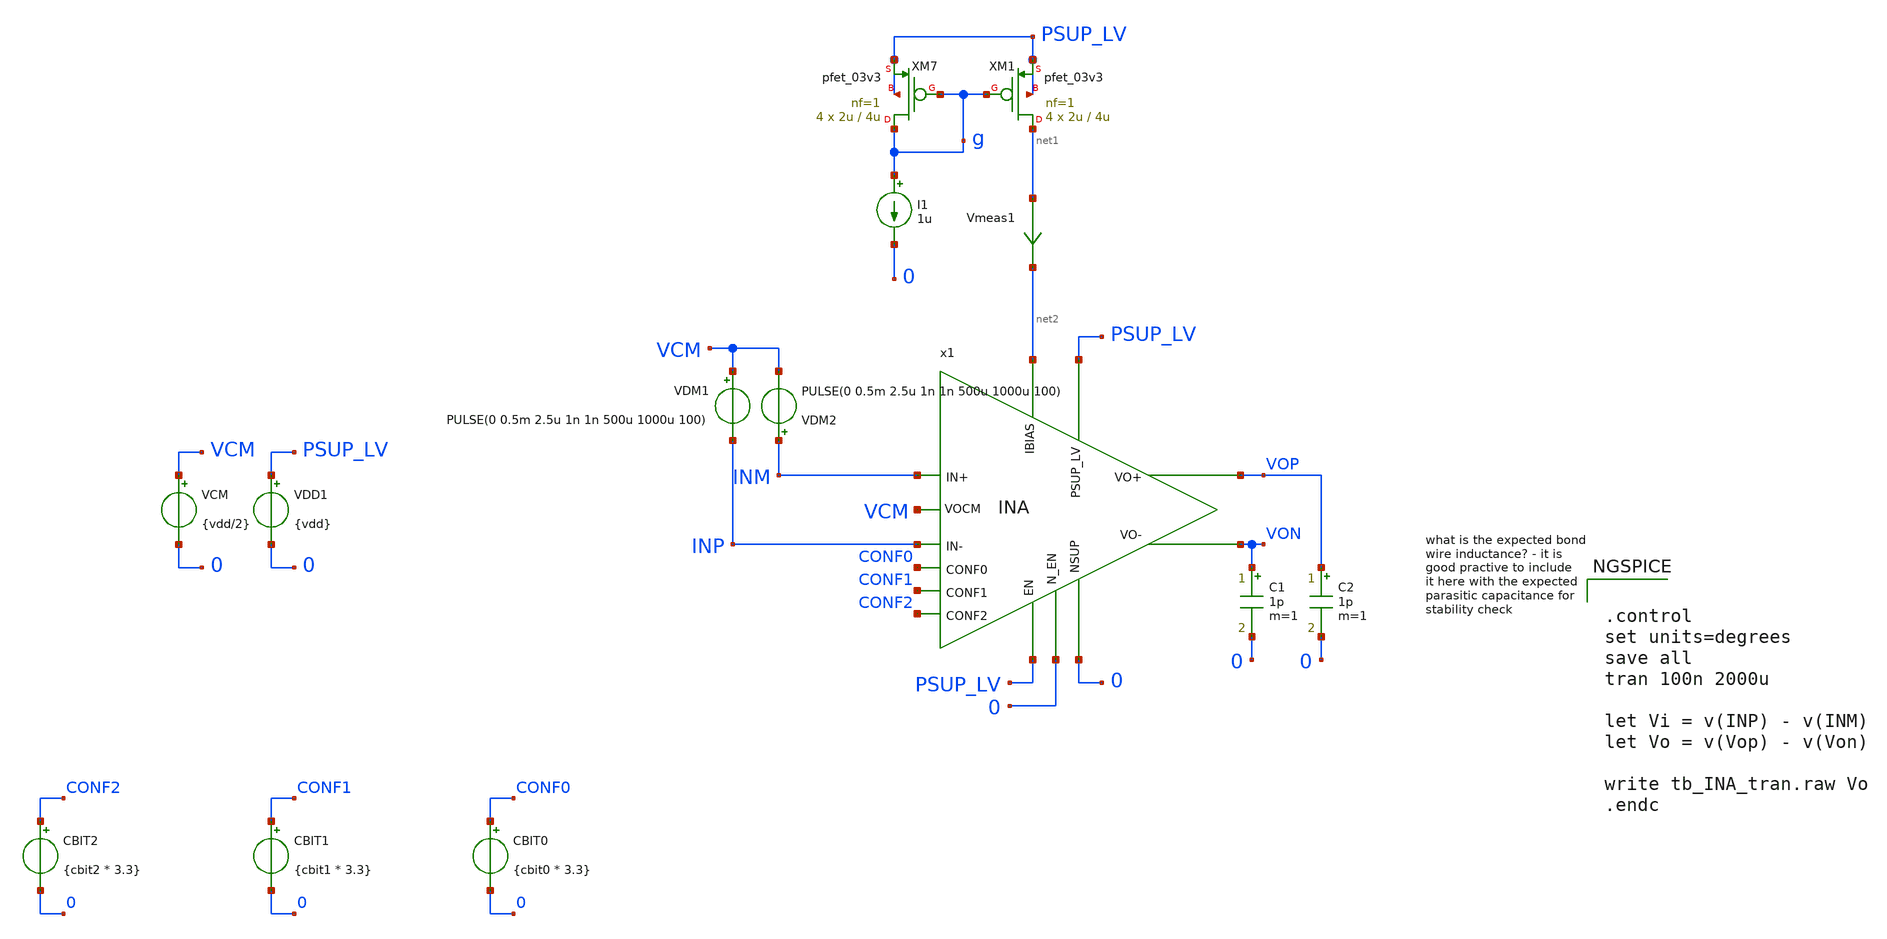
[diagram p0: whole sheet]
** sch_path: xschem/blocks/INA/tb_INA_tran.sch
**.subckt tb_INA_tran
VDD1 PSUP_LV 0 {vdd}
VCM VCM 0 {vdd/2}
VDM2 INM VCM PULSE(0 0.5m 2.5u 1n 1n 500u 1000u 100)
VDM1 VCM INP PULSE(0 0.5m 2.5u 1n 1n 500u 1000u 100)
x1 PSUP_LV 0 PSUP_LV 0 net2 CONF0 CONF1 INM VOP VCM INP VON CONF2 INA
XM7 g g PSUP_LV PSUP_LV pfet_03v3 L=4u W=2u nf=1 ad='int((nf+1)/2) * W/nf * 0.18u' as='int((nf+2)/2) * W/nf * 0.18u'
+ pd='2*int((nf+1)/2) * (W/nf + 0.18u)' ps='2*int((nf+2)/2) * (W/nf + 0.18u)' nrd='0.18u / W' nrs='0.18u / W'
+ sa=0 sb=0 sd=0 m=4
XM1 net1 g PSUP_LV PSUP_LV pfet_03v3 L=4u W=2u nf=1 ad='int((nf+1)/2) * W/nf * 0.18u' as='int((nf+2)/2) * W/nf * 0.18u'
+ pd='2*int((nf+1)/2) * (W/nf + 0.18u)' ps='2*int((nf+2)/2) * (W/nf + 0.18u)' nrd='0.18u / W' nrs='0.18u / W'
+ sa=0 sb=0 sd=0 m=4
I1 g 0 1u
Vmeas1 net1 net2 0
.save i(vmeas1)
C1 VON 0 1p m=1
C2 VOP 0 1p m=1
CBIT1 CONF1 0 {cbit1 * 3.3}
CBIT0 CONF0 0 {cbit0 * 3.3}
CBIT2 CONF2 0 {cbit2 * 3.3}
**** begin user architecture code

.include $::180MCU_MODELS/design.ngspice

.lib $::180MCU_MODELS/sm141064.ngspice typical
.lib $::180MCU_MODELS/sm141064.ngspice res_typical
.lib $::180MCU_MODELS/sm141064.ngspice bjt_typical
.lib $::180MCU_MODELS/sm141064.ngspice mimcap_typical
.lib $::180MCU_MODELS/sm141064.ngspice cap_mim

.temp 25

.param vdd=3.3

.param cbit0=0
.param cbit1=0
.param cbit2=0

* Deterministic PVT: disable random global/mismatch variation.
.param sw_stat_global=0
.param sw_stat_mismatch=0



.control
set units=degrees
save all
tran 100n 2000u

let Vi = v(INP) - v(INM)
let Vo = v(Vop) - v(Von)

write tb_INA_tran.raw Vo
.endc


**** end user architecture code
**.ends
.end
